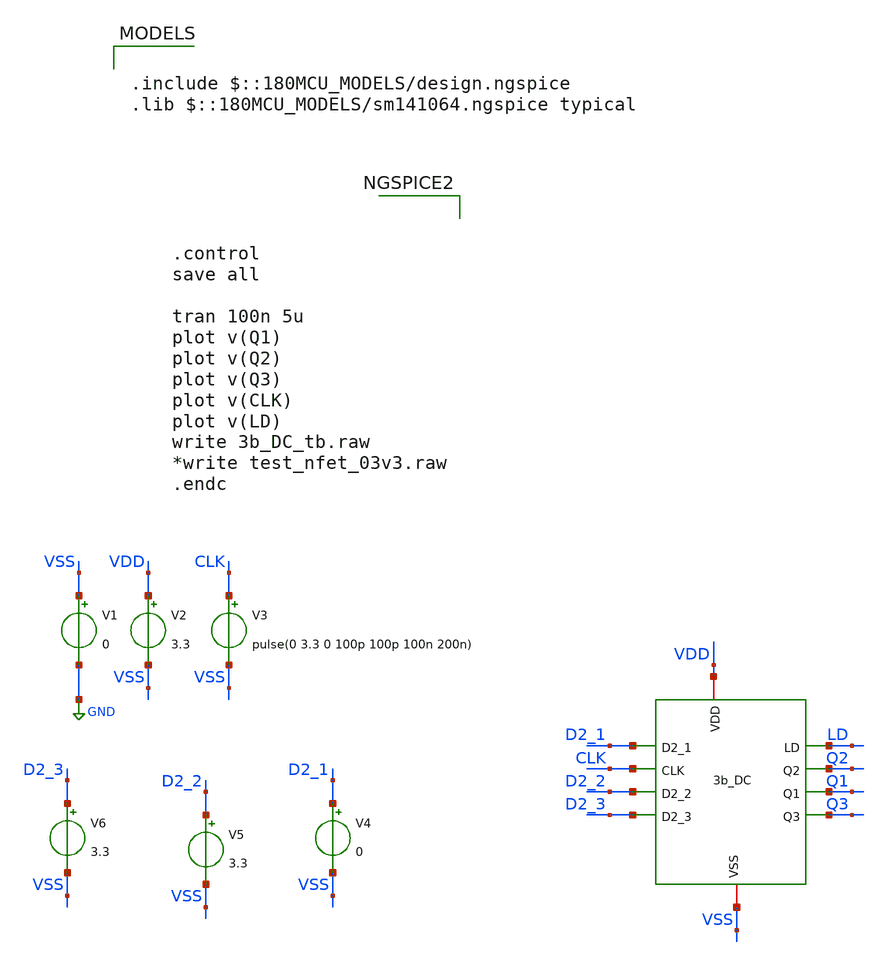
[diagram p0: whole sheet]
** sch_path: Clock_Generator_PAKISTAN_06/Xschem/3b_DC_tb.sch
**.subckt 3b_DC_tb
V1 VSS GND 0
V2 VDD VSS 3.3
V3 CLK VSS pulse(0 3.3 0 100p 100p 100n 200n)
V4 D2_1 VSS 0
V5 D2_2 VSS 3.3
V6 D2_3 VSS 3.3
x1 LD VDD Q2 Q1 Q3 D2_1 CLK VSS D2_2 D2_3 3b_DC
**** begin user architecture code

.include $::180MCU_MODELS/design.ngspice
.lib $::180MCU_MODELS/sm141064.ngspice typical




.control
save all

tran 100n 5u
plot v(Q1)
plot v(Q2)
plot v(Q3)
plot v(CLK)
plot v(LD)
write 3b_DC_tb.raw
*write test_nfet_03v3.raw
.endc


**** end user architecture code
**.ends
.GLOBAL GND
.end
